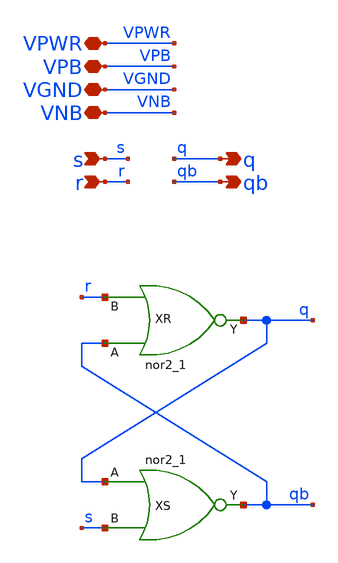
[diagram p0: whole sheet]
** sch_path: xschem/tiny_pll/tiny_pll_pfd_sr_latch.sch
**.subckt tiny_pll_pfd_sr_latch s r q qb VNB VGND VPB VPWR
*.ipin s
*.ipin r
*.opin q
*.opin qb
*.iopin VNB
*.iopin VGND
*.iopin VPB
*.iopin VPWR
XR qb r VGND VNB VPB VPWR q sky130_fd_sc_hd__nor2_1
XS q s VGND VNB VPB VPWR qb sky130_fd_sc_hd__nor2_1
**.ends
.end
